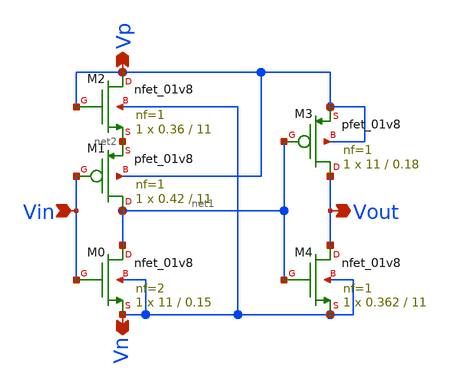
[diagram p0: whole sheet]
** sch_path: xschem/Vth_sch/Symbol/th02.sch
**.subckt th02 Vn Vp Vin Vout
*.opin Vn
*.opin Vp
*.ipin Vin
*.opin Vout
XM3 Vout net1 Vp Vp sky130_fd_pr__pfet_01v8 L=0.18 W=11 nf=1 ad='int((nf+1)/2) * W/nf * 0.29' as='int((nf+2)/2) * W/nf * 0.29'
+ pd='2*int((nf+1)/2) * (W/nf + 0.29)' ps='2*int((nf+2)/2) * (W/nf + 0.29)' nrd='0.29 / W' nrs='0.29 / W'
+ sa=0 sb=0 sd=0 mult=1 m=1
XM4 Vout net1 Vn Vn sky130_fd_pr__nfet_01v8 L=11 W=0.362 nf=1 ad='int((nf+1)/2) * W/nf * 0.29' as='int((nf+2)/2) * W/nf * 0.29'
+ pd='2*int((nf+1)/2) * (W/nf + 0.29)' ps='2*int((nf+2)/2) * (W/nf + 0.29)' nrd='0.29 / W' nrs='0.29 / W'
+ sa=0 sb=0 sd=0 mult=1 m=1
XM1 net1 Vin net2 Vp sky130_fd_pr__pfet_01v8 L=11 W=0.42 nf=1 ad='int((nf+1)/2) * W/nf * 0.29' as='int((nf+2)/2) * W/nf * 0.29'
+ pd='2*int((nf+1)/2) * (W/nf + 0.29)' ps='2*int((nf+2)/2) * (W/nf + 0.29)' nrd='0.29 / W' nrs='0.29 / W'
+ sa=0 sb=0 sd=0 mult=1 m=1
XM0 net1 Vin Vn Vn sky130_fd_pr__nfet_01v8 L=0.15 W=11 nf=2 ad='int((nf+1)/2) * W/nf * 0.29' as='int((nf+2)/2) * W/nf * 0.29'
+ pd='2*int((nf+1)/2) * (W/nf + 0.29)' ps='2*int((nf+2)/2) * (W/nf + 0.29)' nrd='0.29 / W' nrs='0.29 / W'
+ sa=0 sb=0 sd=0 mult=1 m=1
XM2 Vp Vp net2 Vn sky130_fd_pr__nfet_01v8 L=11 W=0.36 nf=1 ad='int((nf+1)/2) * W/nf * 0.29' as='int((nf+2)/2) * W/nf * 0.29'
+ pd='2*int((nf+1)/2) * (W/nf + 0.29)' ps='2*int((nf+2)/2) * (W/nf + 0.29)' nrd='0.29 / W' nrs='0.29 / W'
+ sa=0 sb=0 sd=0 mult=1 m=1
**.ends
.end
